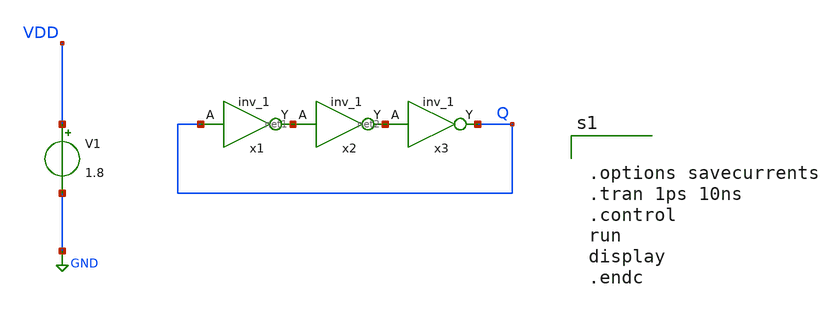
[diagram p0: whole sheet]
** sch_path: xschem/ring_osc.sch
**.subckt ring_osc
V1 VDD GND 1.8
x1 Q GND GND VDD VDD net1 sky130_fd_sc_hd__inv_1
x2 net1 GND GND VDD VDD net2 sky130_fd_sc_hd__inv_1
x3 net2 GND GND VDD VDD Q sky130_fd_sc_hd__inv_1
**** begin user architecture code


.options savecurrents
.tran 1ps 10ns
.control
run
display
.endc

.lib $::SKYWATER_MODELS/sky130.lib.spice ff
.include $::PDKPATH/libs.ref/sky130_fd_sc_hd/spice/sky130_fd_sc_hd.spice

**** end user architecture code
**.ends
.GLOBAL GND
.end
